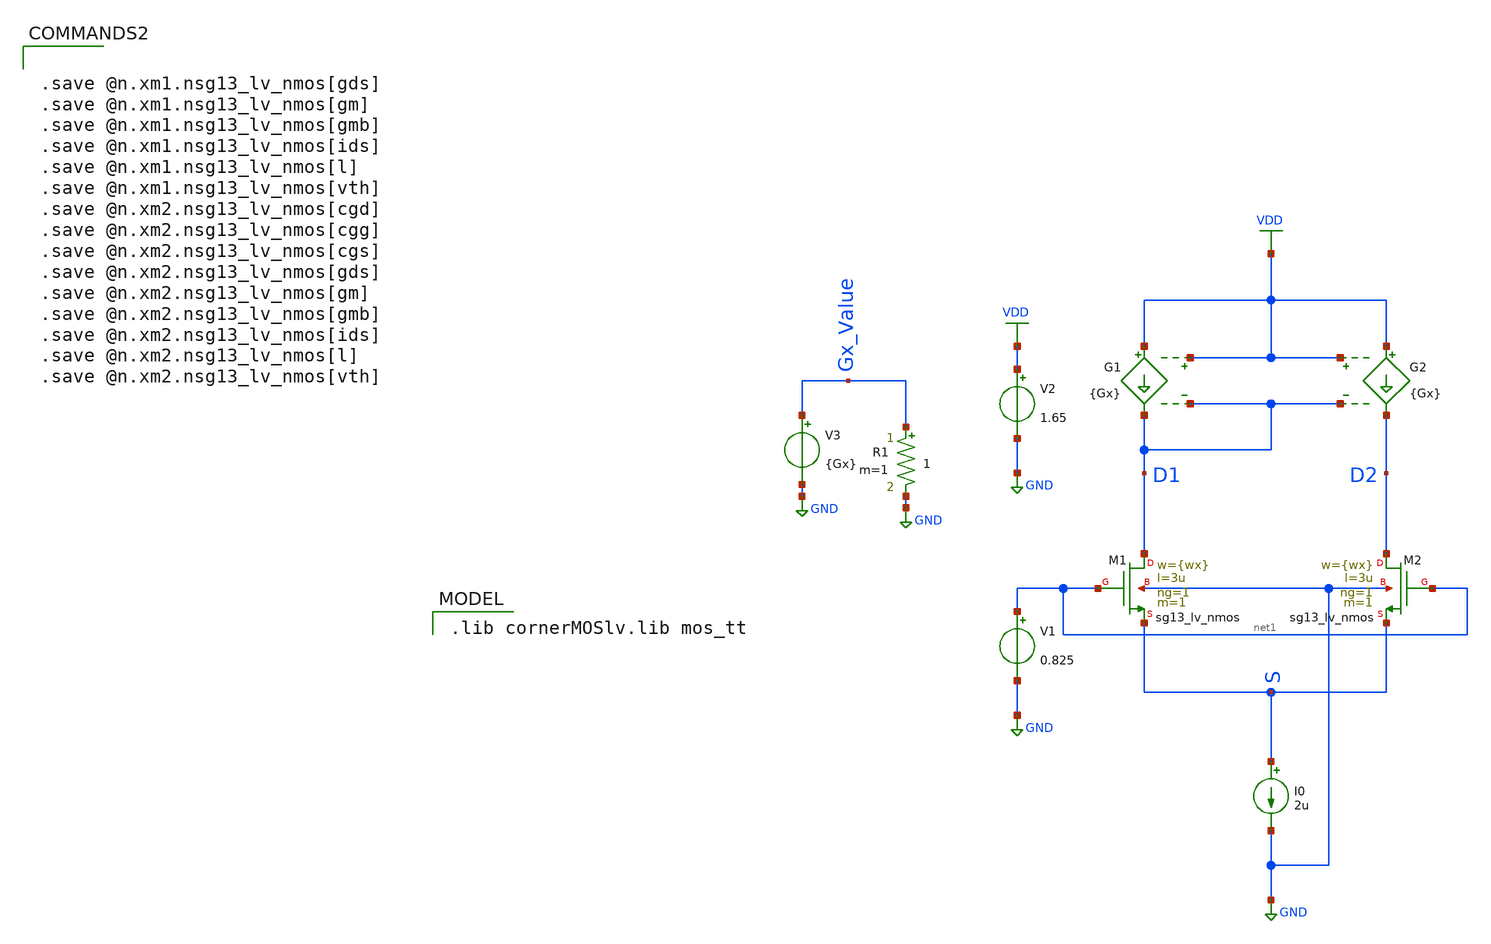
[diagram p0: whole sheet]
** sch_path: VLSI25/submitted_notebooks/Wrøngm/Schematics/Diff-ampwcmfb_test.sch
**.subckt Diff-ampwcmfb_test
I0 S GND 2u
V1 net1 GND 0.825
V2 VDD GND 1.65
G1 VDD D1 VDD D1 {Gx}
G2 VDD D2 VDD D1 {Gx}
XM1 D1 net1 S GND sg13_lv_nmos w={wx} l=3u ng=1 m=1 mm_ok=1
XM2 D2 net1 S GND sg13_lv_nmos w={wx} l=3u ng=1 m=1 mm_ok=1
V3 Gx_Value GND {Gx}
R1 Gx_Value GND 1 m=1
**** begin user architecture code


* ngspice commands
.param wx=0.5u
.param Gx=1u
.options savecurrents

.control
  let start_w = 0.5u
  let stop_w = 20u
  let delta_w = 0.25u

  let start_gx = 1u
  let stop_gx = 10u
  let delta_gx = 1u

  let w_act = start_w

  while w_act le stop_w
    let gx_act = start_gx

    while gx_act le stop_gx
      alterparam wx = $&w_act
      alterparam Gx = $&gx_act

      reset
      save all

      dc v1 0 1.65 0.1

      wrdata /foss/designs/CAC/STG1/Model-1/without-CMFB/5T-OTA/Diff_amp_wcmfb_L3_0.txt
+ @n.xm1.nsg13_lv_nmos[w] v(D1) v(D2) v(S) @n.xm1.nsg13_lv_nmos[gm] @n.xm1.nsg13_lv_nmos[gds] @n.xm1.nsg13_lv_nmos[vgs]
+ @n.xm1.nsg13_lv_nmos[vth] @n.xm1.nsg13_lv_nmos[vsat] @n.xm1.nsg13_lv_nmos[vds] @n.xm1.nsg13_lv_nmos[ids]
+ @n.xm1.nsg13_lv_nmos[cgg] v(Gx_Value)

      let gx_act = gx_act + delta_gx
      set appendwrite
    end

    let w_act = w_act + delta_w
  end
.endc





.save @n.xm1.nsg13_lv_nmos[gds]
.save @n.xm1.nsg13_lv_nmos[gm]
.save @n.xm1.nsg13_lv_nmos[gmb]
.save @n.xm1.nsg13_lv_nmos[ids]
.save @n.xm1.nsg13_lv_nmos[l]
.save @n.xm1.nsg13_lv_nmos[vth]
.save @n.xm2.nsg13_lv_nmos[cgd]
.save @n.xm2.nsg13_lv_nmos[cgg]
.save @n.xm2.nsg13_lv_nmos[cgs]
.save @n.xm2.nsg13_lv_nmos[gds]
.save @n.xm2.nsg13_lv_nmos[gm]
.save @n.xm2.nsg13_lv_nmos[gmb]
.save @n.xm2.nsg13_lv_nmos[ids]
.save @n.xm2.nsg13_lv_nmos[l]
.save @n.xm2.nsg13_lv_nmos[vth]


 .lib cornerMOSlv.lib mos_tt

**** end user architecture code
**.ends
.GLOBAL GND
.GLOBAL VDD
.end
